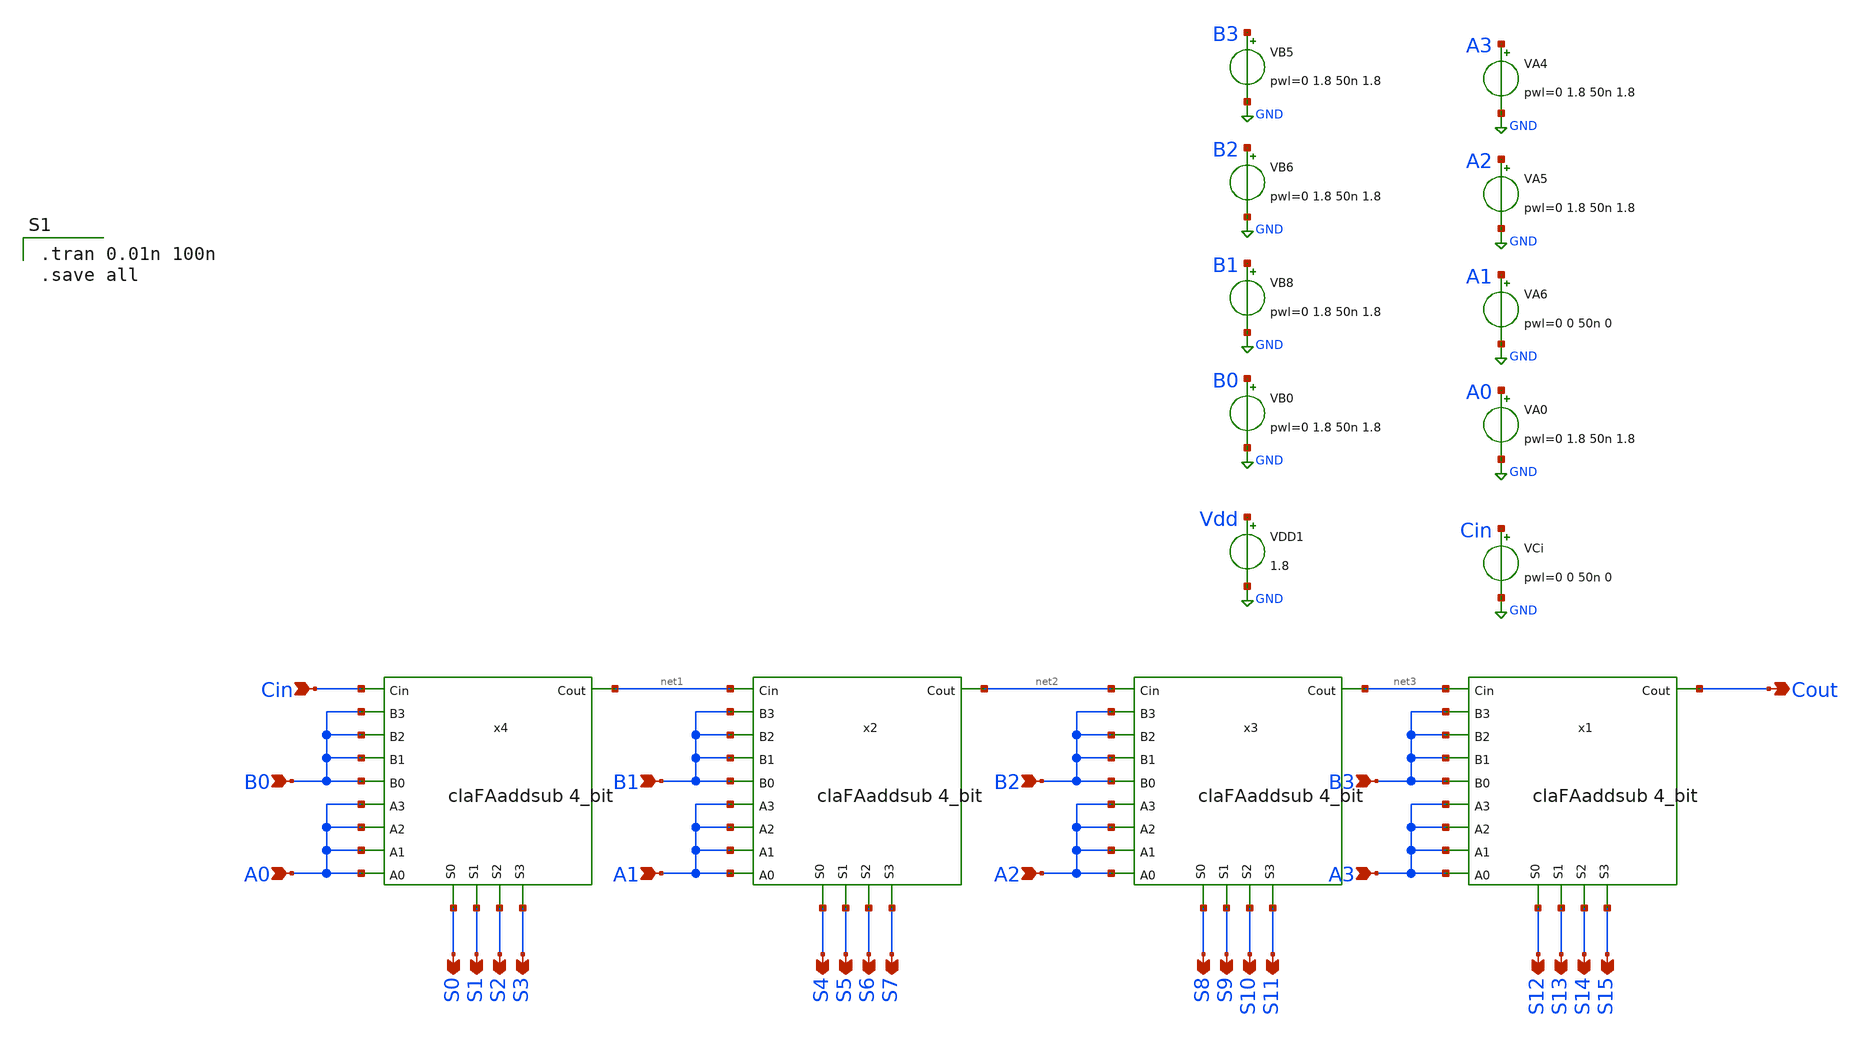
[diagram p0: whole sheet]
** sch_path: gates/32 bit addsubb cla.sch
**.subckt 32 bit addsubb cla B0 A0 B1 A1 B2 A2 B3 A3 S0 S1 S2 S3 S4 S5 S6 S7 S8 S9 S10 S11 S12 S13
*+ S14 S15 Cin Cout
*.ipin B0
*.ipin A0
*.ipin B1
*.ipin A1
*.ipin B2
*.ipin A2
*.ipin B3
*.ipin A3
*.opin S0
*.opin S1
*.opin S2
*.opin S3
*.opin S4
*.opin S5
*.opin S6
*.opin S7
*.opin S8
*.opin S9
*.opin S10
*.opin S11
*.opin S12
*.opin S13
*.opin S14
*.opin S15
*.ipin Cin
*.opin Cout
x1 B3 B3 B3 B3 A3 A3 A3 A3 S14 S13 S12 S15 net3 Cout claFAaddsub 4_bit
x2 B1 B1 B1 B1 A1 A1 A1 A1 S6 S5 S4 S7 net1 net2 claFAaddsub 4_bit
x3 B2 B2 B2 B2 A2 A2 A2 A2 S10 S9 S8 S11 net2 net3 claFAaddsub 4_bit
x4 B0 B0 B0 B0 A0 A0 A0 A0 S2 S1 S0 S3 Cin net1 claFAaddsub 4_bit
VA4 A3 GND pwl=0 1.8 50n 1.8
VA5 A2 GND pwl=0 1.8 50n 1.8
VA6 A1 GND pwl=0 0 50n 0
VA0 A0 GND pwl=0 1.8 50n 1.8
VB5 B3 GND pwl=0 1.8 50n 1.8
VB6 B2 GND pwl=0 1.8 50n 1.8
VB8 B1 GND pwl=0 1.8 50n 1.8
VB0 B0 GND pwl=0 1.8 50n 1.8
VCi Cin GND pwl=0 0 50n 0
VDD1 Vdd GND 1.8
**** begin user architecture code

.tran 0.01n 100n
.save all

.lib $::SKYWATER_MODELS/sky130.lib.spice tt
**** end user architecture code
**.ends

* expanding   symbol:  claFAaddsub 4_bit.sym # of pins=14
** sym_path: gates/claFAaddsub 4_bit.sym
** sch_path: gates/claFAaddsub 4_bit.sch
.subckt claFAaddsub 4_bit B2 B1 B0 B3 A2 A1 A0 A3 S2 S1 S0 S3 Cin Cout
*.opin S0
*.ipin A0
*.ipin B0
*.ipin Cin
*.opin S1
*.ipin A1
*.ipin B1
*.opin S2
*.ipin A2
*.ipin B2
*.opin S3
*.ipin A3
*.ipin B3
*.opin Cout
x1 A0 net4 net3 XOR2
x2 net3 Cin S0 XOR2
x3 net1 Co1 net2 OR2
x4 Cin net1 net3 AND2
x5 A0 net2 net4 AND2
x6 A1 net8 net7 XOR2
x7 net7 C1 S1 XOR2
x8 net5 Co2 net6 OR2
x9 C1 net5 net7 AND2
x10 A1 net6 net8 AND2
x11 A2 net12 net11 XOR2
x12 net11 C2 S2 XOR2
x13 net9 Co3 net10 OR2
x14 C2 net9 net11 AND2
x15 A2 net10 net12 AND2
x16 A3 net14 net13 XOR2
x17 net13 C3 S3 XOR2
x18 net15 Co4 net16 OR2
x19 C3 net15 net13 AND2
x20 A3 net16 net14 AND2
x21 net7 net6 net13 net3 net11 net10 net16 Cin net2 C1 C2 C3 Cout 4_BIT_CLA_Carry_logic
x22 Cin B0 net4 XOR2
x23 Cin B1 net8 XOR2
x24 Cin B2 net12 XOR2
x25 Cin B3 net14 XOR2
.ends


* expanding   symbol:  XOR2.sym # of pins=3
** sym_path: gates/XOR2.sym
** sch_path: gates/XOR2.sch
.subckt XOR2 B A Y
*.ipin A
*.ipin B
*.opin Y
XM1 Y A net5 GND sky130_fd_pr__nfet_01v8 L=0.15 W=1 nf=1 ad='int((nf+1)/2) * W/nf * 0.29' as='int((nf+2)/2) * W/nf * 0.29'
+ pd='2*int((nf+1)/2) * (W/nf + 0.29)' ps='2*int((nf+2)/2) * (W/nf + 0.29)' nrd='0.29 / W' nrs='0.29 / W'
+ sa=0 sb=0 sd=0 mult=1 m=1
XM2 net5 B GND GND sky130_fd_pr__nfet_01v8 L=0.15 W=1 nf=1 ad='int((nf+1)/2) * W/nf * 0.29' as='int((nf+2)/2) * W/nf * 0.29'
+ pd='2*int((nf+1)/2) * (W/nf + 0.29)' ps='2*int((nf+2)/2) * (W/nf + 0.29)' nrd='0.29 / W' nrs='0.29 / W'
+ sa=0 sb=0 sd=0 mult=1 m=1
XM3 Y net1 net2 VDD sky130_fd_pr__pfet_01v8 L=0.15 W=1 nf=1 ad='int((nf+1)/2) * W/nf * 0.29' as='int((nf+2)/2) * W/nf * 0.29'
+ pd='2*int((nf+1)/2) * (W/nf + 0.29)' ps='2*int((nf+2)/2) * (W/nf + 0.29)' nrd='0.29 / W' nrs='0.29 / W'
+ sa=0 sb=0 sd=0 mult=1 m=1
XM4 net2 A VDD VDD sky130_fd_pr__pfet_01v8 L=0.15 W=1 nf=1 ad='int((nf+1)/2) * W/nf * 0.29' as='int((nf+2)/2) * W/nf * 0.29'
+ pd='2*int((nf+1)/2) * (W/nf + 0.29)' ps='2*int((nf+2)/2) * (W/nf + 0.29)' nrd='0.29 / W' nrs='0.29 / W'
+ sa=0 sb=0 sd=0 mult=1 m=1
XM5 net2 B VDD VDD sky130_fd_pr__pfet_01v8 L=0.15 W=1 nf=1 ad='int((nf+1)/2) * W/nf * 0.29' as='int((nf+2)/2) * W/nf * 0.29'
+ pd='2*int((nf+1)/2) * (W/nf + 0.29)' ps='2*int((nf+2)/2) * (W/nf + 0.29)' nrd='0.29 / W' nrs='0.29 / W'
+ sa=0 sb=0 sd=0 mult=1 m=1
XM6 Y net3 net2 VDD sky130_fd_pr__pfet_01v8 L=0.15 W=1 nf=1 ad='int((nf+1)/2) * W/nf * 0.29' as='int((nf+2)/2) * W/nf * 0.29'
+ pd='2*int((nf+1)/2) * (W/nf + 0.29)' ps='2*int((nf+2)/2) * (W/nf + 0.29)' nrd='0.29 / W' nrs='0.29 / W'
+ sa=0 sb=0 sd=0 mult=1 m=1
XM7 Y net1 net4 GND sky130_fd_pr__nfet_01v8 L=0.15 W=1 nf=1 ad='int((nf+1)/2) * W/nf * 0.29' as='int((nf+2)/2) * W/nf * 0.29'
+ pd='2*int((nf+1)/2) * (W/nf + 0.29)' ps='2*int((nf+2)/2) * (W/nf + 0.29)' nrd='0.29 / W' nrs='0.29 / W'
+ sa=0 sb=0 sd=0 mult=1 m=1
XM8 net4 net3 GND GND sky130_fd_pr__nfet_01v8 L=0.15 W=1 nf=1 ad='int((nf+1)/2) * W/nf * 0.29' as='int((nf+2)/2) * W/nf * 0.29'
+ pd='2*int((nf+1)/2) * (W/nf + 0.29)' ps='2*int((nf+2)/2) * (W/nf + 0.29)' nrd='0.29 / W' nrs='0.29 / W'
+ sa=0 sb=0 sd=0 mult=1 m=1
X1 A net1 inv_vtc
X2 B net3 inv_vtc
.ends


* expanding   symbol:  OR2.sym # of pins=3
** sym_path: gates/OR2.sym
** sch_path: gates/OR2.sch
.subckt OR2 B Y A
*.ipin A
*.ipin B
*.opin Y
XM7 VDD B net2 VDD sky130_fd_pr__pfet_01v8 L=0.15 W=1 nf=1 ad='int((nf+1)/2) * W/nf * 0.29' as='int((nf+2)/2) * W/nf * 0.29'
+ pd='2*int((nf+1)/2) * (W/nf + 0.29)' ps='2*int((nf+2)/2) * (W/nf + 0.29)' nrd='0.29 / W' nrs='0.29 / W'
+ sa=0 sb=0 sd=0 mult=1 m=1
XM8 GND B net1 GND sky130_fd_pr__nfet_01v8 L=0.15 W=1 nf=1 ad='int((nf+1)/2) * W/nf * 0.29' as='int((nf+2)/2) * W/nf * 0.29'
+ pd='2*int((nf+1)/2) * (W/nf + 0.29)' ps='2*int((nf+2)/2) * (W/nf + 0.29)' nrd='0.29 / W' nrs='0.29 / W'
+ sa=0 sb=0 sd=0 mult=1 m=1
XM9 net2 A net1 VDD sky130_fd_pr__pfet_01v8 L=0.15 W=1 nf=1 ad='int((nf+1)/2) * W/nf * 0.29' as='int((nf+2)/2) * W/nf * 0.29'
+ pd='2*int((nf+1)/2) * (W/nf + 0.29)' ps='2*int((nf+2)/2) * (W/nf + 0.29)' nrd='0.29 / W' nrs='0.29 / W'
+ sa=0 sb=0 sd=0 mult=1 m=1
XM10 GND A net1 GND sky130_fd_pr__nfet_01v8 L=0.15 W=1 nf=1 ad='int((nf+1)/2) * W/nf * 0.29' as='int((nf+2)/2) * W/nf * 0.29'
+ pd='2*int((nf+1)/2) * (W/nf + 0.29)' ps='2*int((nf+2)/2) * (W/nf + 0.29)' nrd='0.29 / W' nrs='0.29 / W'
+ sa=0 sb=0 sd=0 mult=1 m=1
X1 net1 Y inv_vtc
.ends


* expanding   symbol:  AND2.sym # of pins=3
** sym_path: gates/AND2.sym
** sch_path: gates/AND2.sch
.subckt AND2 A Y B
*.opin Y
*.ipin A
*.ipin B
x1 A net1 B NAND2_Gate
X2 net1 Y inv_vtc
.ends


* expanding   symbol:  4_BIT_CLA_Carry_logic.sym # of pins=13
** sym_path: gates/4_BIT_CLA_Carry_logic.sym
** sch_path: gates/4_BIT_CLA_Carry_logic.sch
.subckt 4_BIT_CLA_Carry_logic P1 G1 P3 P0 P2 G2 G3 Cin G0 C1 C2 C3 C4
*.ipin P0
*.ipin P1
*.ipin P2
*.ipin P3
*.ipin G0
*.ipin G1
*.ipin G2
*.ipin G3
*.ipin Cin
*.opin C1
*.opin C2
*.opin C3
*.opin C4
x5 Cin x5 P0 AND2
x6 G0 C1 x5 OR2
x7 G1 net1 net2 C2 OR3
x8 P1 net1 G0 AND2
x9 Cin net10 P0 P1 AND3
x1 G2 net3 net4 C3 net5 OR4
x2 P2 net3 G1 AND2
x3 P1 net11 P2 G0 AND3
x4 net12 net5 net13 net14 net15 AND4
x10 G3 net6 net7 net8 C4 net9 OR5
x12 P3 net6 G2 AND2
x13 net16 net17 net18 net19 AND3
x14 net20 net8 net21 net22 net23 AND4
x11 net24 net25 net26 net27 net28 net29 AND5
.ends


* expanding   symbol:  inv_vtc.sym # of pins=2
** sym_path: gates/inv_vtc.sym
** sch_path: gates/inv_vtc.sch
.subckt inv_vtc A Y
*.ipin A
*.opin Y
XM1 Y A VDD VDD sky130_fd_pr__pfet_01v8 L=0.15 W=2 nf=1 ad='int((nf+1)/2) * W/nf * 0.29' as='int((nf+2)/2) * W/nf * 0.29'
+ pd='2*int((nf+1)/2) * (W/nf + 0.29)' ps='2*int((nf+2)/2) * (W/nf + 0.29)' nrd='0.29 / W' nrs='0.29 / W'
+ sa=0 sb=0 sd=0 mult=1 m=1
XM2 Y A GND GND sky130_fd_pr__nfet_01v8 L=0.15 W=1 nf=1 ad='int((nf+1)/2) * W/nf * 0.29' as='int((nf+2)/2) * W/nf * 0.29'
+ pd='2*int((nf+1)/2) * (W/nf + 0.29)' ps='2*int((nf+2)/2) * (W/nf + 0.29)' nrd='0.29 / W' nrs='0.29 / W'
+ sa=0 sb=0 sd=0 mult=1 m=1
.ends


* expanding   symbol:  NAND2_Gate.sym # of pins=3
** sym_path: gates/NAND2_Gate.sym
** sch_path: gates/NAND2_Gate.sch
.subckt NAND2_Gate A Y B
*.ipin A
*.ipin B
*.opin Y
XM1 Y A net1 GND sky130_fd_pr__nfet_01v8 L=0.15 W=1 nf=1 ad='int((nf+1)/2) * W/nf * 0.29' as='int((nf+2)/2) * W/nf * 0.29'
+ pd='2*int((nf+1)/2) * (W/nf + 0.29)' ps='2*int((nf+2)/2) * (W/nf + 0.29)' nrd='0.29 / W' nrs='0.29 / W'
+ sa=0 sb=0 sd=0 mult=1 m=1
XM2 net1 B GND GND sky130_fd_pr__nfet_01v8 L=0.15 W=1 nf=1 ad='int((nf+1)/2) * W/nf * 0.29' as='int((nf+2)/2) * W/nf * 0.29'
+ pd='2*int((nf+1)/2) * (W/nf + 0.29)' ps='2*int((nf+2)/2) * (W/nf + 0.29)' nrd='0.29 / W' nrs='0.29 / W'
+ sa=0 sb=0 sd=0 mult=1 m=1
XM3 Y A VDD VDD sky130_fd_pr__pfet_01v8 L=0.15 W=1 nf=1 ad='int((nf+1)/2) * W/nf * 0.29' as='int((nf+2)/2) * W/nf * 0.29'
+ pd='2*int((nf+1)/2) * (W/nf + 0.29)' ps='2*int((nf+2)/2) * (W/nf + 0.29)' nrd='0.29 / W' nrs='0.29 / W'
+ sa=0 sb=0 sd=0 mult=1 m=1
XM4 Y B VDD VDD sky130_fd_pr__pfet_01v8 L=0.15 W=1 nf=1 ad='int((nf+1)/2) * W/nf * 0.29' as='int((nf+2)/2) * W/nf * 0.29'
+ pd='2*int((nf+1)/2) * (W/nf + 0.29)' ps='2*int((nf+2)/2) * (W/nf + 0.29)' nrd='0.29 / W' nrs='0.29 / W'
+ sa=0 sb=0 sd=0 mult=1 m=1
.ends


* expanding   symbol:  OR3.sym # of pins=4
** sym_path: gates/OR3.sym
** sch_path: gates/OR3.sch
.subckt OR3 C B A Y
*.ipin A
*.ipin B
*.opin Y
*.ipin C
XM5 VDD C net3 VDD sky130_fd_pr__pfet_01v8 L=0.15 W=1 nf=1 ad='int((nf+1)/2) * W/nf * 0.29' as='int((nf+2)/2) * W/nf * 0.29'
+ pd='2*int((nf+1)/2) * (W/nf + 0.29)' ps='2*int((nf+2)/2) * (W/nf + 0.29)' nrd='0.29 / W' nrs='0.29 / W'
+ sa=0 sb=0 sd=0 mult=1 m=1
XM6 GND C net1 GND sky130_fd_pr__nfet_01v8 L=0.15 W=1 nf=1 ad='int((nf+1)/2) * W/nf * 0.29' as='int((nf+2)/2) * W/nf * 0.29'
+ pd='2*int((nf+1)/2) * (W/nf + 0.29)' ps='2*int((nf+2)/2) * (W/nf + 0.29)' nrd='0.29 / W' nrs='0.29 / W'
+ sa=0 sb=0 sd=0 mult=1 m=1
XM7 net3 B net2 VDD sky130_fd_pr__pfet_01v8 L=0.15 W=1 nf=1 ad='int((nf+1)/2) * W/nf * 0.29' as='int((nf+2)/2) * W/nf * 0.29'
+ pd='2*int((nf+1)/2) * (W/nf + 0.29)' ps='2*int((nf+2)/2) * (W/nf + 0.29)' nrd='0.29 / W' nrs='0.29 / W'
+ sa=0 sb=0 sd=0 mult=1 m=1
XM8 GND B net1 GND sky130_fd_pr__nfet_01v8 L=0.15 W=1 nf=1 ad='int((nf+1)/2) * W/nf * 0.29' as='int((nf+2)/2) * W/nf * 0.29'
+ pd='2*int((nf+1)/2) * (W/nf + 0.29)' ps='2*int((nf+2)/2) * (W/nf + 0.29)' nrd='0.29 / W' nrs='0.29 / W'
+ sa=0 sb=0 sd=0 mult=1 m=1
XM9 net2 A net1 VDD sky130_fd_pr__pfet_01v8 L=0.15 W=1 nf=1 ad='int((nf+1)/2) * W/nf * 0.29' as='int((nf+2)/2) * W/nf * 0.29'
+ pd='2*int((nf+1)/2) * (W/nf + 0.29)' ps='2*int((nf+2)/2) * (W/nf + 0.29)' nrd='0.29 / W' nrs='0.29 / W'
+ sa=0 sb=0 sd=0 mult=1 m=1
XM10 GND A net1 GND sky130_fd_pr__nfet_01v8 L=0.15 W=1 nf=1 ad='int((nf+1)/2) * W/nf * 0.29' as='int((nf+2)/2) * W/nf * 0.29'
+ pd='2*int((nf+1)/2) * (W/nf + 0.29)' ps='2*int((nf+2)/2) * (W/nf + 0.29)' nrd='0.29 / W' nrs='0.29 / W'
+ sa=0 sb=0 sd=0 mult=1 m=1
X1 net1 Y inv_vtc
.ends


* expanding   symbol:  AND3.sym # of pins=4
** sym_path: gates/AND3.sym
** sch_path: gates/AND3.sch
.subckt AND3 A Y B c
*.ipin A
*.ipin B
*.opin Y
*.ipin c
XM1 net1 A net2 GND sky130_fd_pr__nfet_01v8 L=0.15 W=1 nf=1 ad='int((nf+1)/2) * W/nf * 0.29' as='int((nf+2)/2) * W/nf * 0.29'
+ pd='2*int((nf+1)/2) * (W/nf + 0.29)' ps='2*int((nf+2)/2) * (W/nf + 0.29)' nrd='0.29 / W' nrs='0.29 / W'
+ sa=0 sb=0 sd=0 mult=1 m=1
XM2 net2 B net3 GND sky130_fd_pr__nfet_01v8 L=0.15 W=1 nf=1 ad='int((nf+1)/2) * W/nf * 0.29' as='int((nf+2)/2) * W/nf * 0.29'
+ pd='2*int((nf+1)/2) * (W/nf + 0.29)' ps='2*int((nf+2)/2) * (W/nf + 0.29)' nrd='0.29 / W' nrs='0.29 / W'
+ sa=0 sb=0 sd=0 mult=1 m=1
XM3 net1 A VDD VDD sky130_fd_pr__pfet_01v8 L=0.15 W=1 nf=1 ad='int((nf+1)/2) * W/nf * 0.29' as='int((nf+2)/2) * W/nf * 0.29'
+ pd='2*int((nf+1)/2) * (W/nf + 0.29)' ps='2*int((nf+2)/2) * (W/nf + 0.29)' nrd='0.29 / W' nrs='0.29 / W'
+ sa=0 sb=0 sd=0 mult=1 m=1
XM4 net1 B VDD VDD sky130_fd_pr__pfet_01v8 L=0.15 W=1 nf=1 ad='int((nf+1)/2) * W/nf * 0.29' as='int((nf+2)/2) * W/nf * 0.29'
+ pd='2*int((nf+1)/2) * (W/nf + 0.29)' ps='2*int((nf+2)/2) * (W/nf + 0.29)' nrd='0.29 / W' nrs='0.29 / W'
+ sa=0 sb=0 sd=0 mult=1 m=1
XM5 net1 c VDD VDD sky130_fd_pr__pfet_01v8 L=0.15 W=1 nf=1 ad='int((nf+1)/2) * W/nf * 0.29' as='int((nf+2)/2) * W/nf * 0.29'
+ pd='2*int((nf+1)/2) * (W/nf + 0.29)' ps='2*int((nf+2)/2) * (W/nf + 0.29)' nrd='0.29 / W' nrs='0.29 / W'
+ sa=0 sb=0 sd=0 mult=1 m=1
XM6 net3 c GND GND sky130_fd_pr__nfet_01v8 L=0.15 W=1 nf=1 ad='int((nf+1)/2) * W/nf * 0.29' as='int((nf+2)/2) * W/nf * 0.29'
+ pd='2*int((nf+1)/2) * (W/nf + 0.29)' ps='2*int((nf+2)/2) * (W/nf + 0.29)' nrd='0.29 / W' nrs='0.29 / W'
+ sa=0 sb=0 sd=0 mult=1 m=1
X1 net1 Y inv_vtc
.ends


* expanding   symbol:  OR4.sym # of pins=5
** sym_path: gates/OR4.sym
** sch_path: gates/OR4.sch
.subckt OR4 D C B Y A
*.ipin A
*.ipin B
*.opin Y
*.ipin C
*.ipin D
XM2 GND D net1 GND sky130_fd_pr__nfet_01v8 L=0.15 W=1 nf=1 ad='int((nf+1)/2) * W/nf * 0.29' as='int((nf+2)/2) * W/nf * 0.29'
+ pd='2*int((nf+1)/2) * (W/nf + 0.29)' ps='2*int((nf+2)/2) * (W/nf + 0.29)' nrd='0.29 / W' nrs='0.29 / W'
+ sa=0 sb=0 sd=0 mult=1 m=1
XM4 VDD D net4 VDD sky130_fd_pr__pfet_01v8 L=0.15 W=1 nf=1 ad='int((nf+1)/2) * W/nf * 0.29' as='int((nf+2)/2) * W/nf * 0.29'
+ pd='2*int((nf+1)/2) * (W/nf + 0.29)' ps='2*int((nf+2)/2) * (W/nf + 0.29)' nrd='0.29 / W' nrs='0.29 / W'
+ sa=0 sb=0 sd=0 mult=1 m=1
XM5 net4 C net3 VDD sky130_fd_pr__pfet_01v8 L=0.15 W=1 nf=1 ad='int((nf+1)/2) * W/nf * 0.29' as='int((nf+2)/2) * W/nf * 0.29'
+ pd='2*int((nf+1)/2) * (W/nf + 0.29)' ps='2*int((nf+2)/2) * (W/nf + 0.29)' nrd='0.29 / W' nrs='0.29 / W'
+ sa=0 sb=0 sd=0 mult=1 m=1
XM6 GND C net1 GND sky130_fd_pr__nfet_01v8 L=0.15 W=1 nf=1 ad='int((nf+1)/2) * W/nf * 0.29' as='int((nf+2)/2) * W/nf * 0.29'
+ pd='2*int((nf+1)/2) * (W/nf + 0.29)' ps='2*int((nf+2)/2) * (W/nf + 0.29)' nrd='0.29 / W' nrs='0.29 / W'
+ sa=0 sb=0 sd=0 mult=1 m=1
XM7 net3 B net2 VDD sky130_fd_pr__pfet_01v8 L=0.15 W=1 nf=1 ad='int((nf+1)/2) * W/nf * 0.29' as='int((nf+2)/2) * W/nf * 0.29'
+ pd='2*int((nf+1)/2) * (W/nf + 0.29)' ps='2*int((nf+2)/2) * (W/nf + 0.29)' nrd='0.29 / W' nrs='0.29 / W'
+ sa=0 sb=0 sd=0 mult=1 m=1
XM8 GND B net1 GND sky130_fd_pr__nfet_01v8 L=0.15 W=1 nf=1 ad='int((nf+1)/2) * W/nf * 0.29' as='int((nf+2)/2) * W/nf * 0.29'
+ pd='2*int((nf+1)/2) * (W/nf + 0.29)' ps='2*int((nf+2)/2) * (W/nf + 0.29)' nrd='0.29 / W' nrs='0.29 / W'
+ sa=0 sb=0 sd=0 mult=1 m=1
XM9 net2 A net1 VDD sky130_fd_pr__pfet_01v8 L=0.15 W=1 nf=1 ad='int((nf+1)/2) * W/nf * 0.29' as='int((nf+2)/2) * W/nf * 0.29'
+ pd='2*int((nf+1)/2) * (W/nf + 0.29)' ps='2*int((nf+2)/2) * (W/nf + 0.29)' nrd='0.29 / W' nrs='0.29 / W'
+ sa=0 sb=0 sd=0 mult=1 m=1
XM10 GND A net1 GND sky130_fd_pr__nfet_01v8 L=0.15 W=1 nf=1 ad='int((nf+1)/2) * W/nf * 0.29' as='int((nf+2)/2) * W/nf * 0.29'
+ pd='2*int((nf+1)/2) * (W/nf + 0.29)' ps='2*int((nf+2)/2) * (W/nf + 0.29)' nrd='0.29 / W' nrs='0.29 / W'
+ sa=0 sb=0 sd=0 mult=1 m=1
X2 net1 Y inv_vtc
.ends


* expanding   symbol:  AND4.sym # of pins=5
** sym_path: gates/AND4.sym
** sch_path: gates/AND4.sch
.subckt AND4 A Y B C D
*.ipin A
*.ipin B
*.opin Y
*.ipin C
*.ipin D
XM1 net1 A net2 GND sky130_fd_pr__nfet_01v8 L=0.15 W=1 nf=1 ad='int((nf+1)/2) * W/nf * 0.29' as='int((nf+2)/2) * W/nf * 0.29'
+ pd='2*int((nf+1)/2) * (W/nf + 0.29)' ps='2*int((nf+2)/2) * (W/nf + 0.29)' nrd='0.29 / W' nrs='0.29 / W'
+ sa=0 sb=0 sd=0 mult=1 m=1
XM2 net2 B net3 GND sky130_fd_pr__nfet_01v8 L=0.15 W=1 nf=1 ad='int((nf+1)/2) * W/nf * 0.29' as='int((nf+2)/2) * W/nf * 0.29'
+ pd='2*int((nf+1)/2) * (W/nf + 0.29)' ps='2*int((nf+2)/2) * (W/nf + 0.29)' nrd='0.29 / W' nrs='0.29 / W'
+ sa=0 sb=0 sd=0 mult=1 m=1
XM3 net1 A VDD VDD sky130_fd_pr__pfet_01v8 L=0.15 W=1 nf=1 ad='int((nf+1)/2) * W/nf * 0.29' as='int((nf+2)/2) * W/nf * 0.29'
+ pd='2*int((nf+1)/2) * (W/nf + 0.29)' ps='2*int((nf+2)/2) * (W/nf + 0.29)' nrd='0.29 / W' nrs='0.29 / W'
+ sa=0 sb=0 sd=0 mult=1 m=1
XM4 net1 B VDD VDD sky130_fd_pr__pfet_01v8 L=0.15 W=1 nf=1 ad='int((nf+1)/2) * W/nf * 0.29' as='int((nf+2)/2) * W/nf * 0.29'
+ pd='2*int((nf+1)/2) * (W/nf + 0.29)' ps='2*int((nf+2)/2) * (W/nf + 0.29)' nrd='0.29 / W' nrs='0.29 / W'
+ sa=0 sb=0 sd=0 mult=1 m=1
XM5 net1 C VDD VDD sky130_fd_pr__pfet_01v8 L=0.15 W=1 nf=1 ad='int((nf+1)/2) * W/nf * 0.29' as='int((nf+2)/2) * W/nf * 0.29'
+ pd='2*int((nf+1)/2) * (W/nf + 0.29)' ps='2*int((nf+2)/2) * (W/nf + 0.29)' nrd='0.29 / W' nrs='0.29 / W'
+ sa=0 sb=0 sd=0 mult=1 m=1
XM6 net3 C net4 GND sky130_fd_pr__nfet_01v8 L=0.15 W=1 nf=1 ad='int((nf+1)/2) * W/nf * 0.29' as='int((nf+2)/2) * W/nf * 0.29'
+ pd='2*int((nf+1)/2) * (W/nf + 0.29)' ps='2*int((nf+2)/2) * (W/nf + 0.29)' nrd='0.29 / W' nrs='0.29 / W'
+ sa=0 sb=0 sd=0 mult=1 m=1
XM7 net1 D VDD VDD sky130_fd_pr__pfet_01v8 L=0.15 W=1 nf=1 ad='int((nf+1)/2) * W/nf * 0.29' as='int((nf+2)/2) * W/nf * 0.29'
+ pd='2*int((nf+1)/2) * (W/nf + 0.29)' ps='2*int((nf+2)/2) * (W/nf + 0.29)' nrd='0.29 / W' nrs='0.29 / W'
+ sa=0 sb=0 sd=0 mult=1 m=1
XM8 net4 D GND GND sky130_fd_pr__nfet_01v8 L=0.15 W=1 nf=1 ad='int((nf+1)/2) * W/nf * 0.29' as='int((nf+2)/2) * W/nf * 0.29'
+ pd='2*int((nf+1)/2) * (W/nf + 0.29)' ps='2*int((nf+2)/2) * (W/nf + 0.29)' nrd='0.29 / W' nrs='0.29 / W'
+ sa=0 sb=0 sd=0 mult=1 m=1
X1 net1 Y inv_vtc
.ends


* expanding   symbol:  OR5.sym # of pins=6
** sym_path: gates/OR5.sym
** sch_path: gates/OR5.sch
.subckt OR5 E D C B Y A
*.ipin A
*.ipin B
*.opin Y
*.ipin C
*.ipin D
*.ipin E
XM1 GND E net1 GND sky130_fd_pr__nfet_01v8 L=0.15 W=1 nf=1 ad='int((nf+1)/2) * W/nf * 0.29' as='int((nf+2)/2) * W/nf * 0.29'
+ pd='2*int((nf+1)/2) * (W/nf + 0.29)' ps='2*int((nf+2)/2) * (W/nf + 0.29)' nrd='0.29 / W' nrs='0.29 / W'
+ sa=0 sb=0 sd=0 mult=1 m=1
XM2 GND D net1 GND sky130_fd_pr__nfet_01v8 L=0.15 W=1 nf=1 ad='int((nf+1)/2) * W/nf * 0.29' as='int((nf+2)/2) * W/nf * 0.29'
+ pd='2*int((nf+1)/2) * (W/nf + 0.29)' ps='2*int((nf+2)/2) * (W/nf + 0.29)' nrd='0.29 / W' nrs='0.29 / W'
+ sa=0 sb=0 sd=0 mult=1 m=1
XM3 VDD E VDD VDD sky130_fd_pr__pfet_01v8 L=0.15 W=1 nf=1 ad='int((nf+1)/2) * W/nf * 0.29' as='int((nf+2)/2) * W/nf * 0.29'
+ pd='2*int((nf+1)/2) * (W/nf + 0.29)' ps='2*int((nf+2)/2) * (W/nf + 0.29)' nrd='0.29 / W' nrs='0.29 / W'
+ sa=0 sb=0 sd=0 mult=1 m=1
XM4 VDD D net4 VDD sky130_fd_pr__pfet_01v8 L=0.15 W=1 nf=1 ad='int((nf+1)/2) * W/nf * 0.29' as='int((nf+2)/2) * W/nf * 0.29'
+ pd='2*int((nf+1)/2) * (W/nf + 0.29)' ps='2*int((nf+2)/2) * (W/nf + 0.29)' nrd='0.29 / W' nrs='0.29 / W'
+ sa=0 sb=0 sd=0 mult=1 m=1
XM5 net4 C net3 VDD sky130_fd_pr__pfet_01v8 L=0.15 W=1 nf=1 ad='int((nf+1)/2) * W/nf * 0.29' as='int((nf+2)/2) * W/nf * 0.29'
+ pd='2*int((nf+1)/2) * (W/nf + 0.29)' ps='2*int((nf+2)/2) * (W/nf + 0.29)' nrd='0.29 / W' nrs='0.29 / W'
+ sa=0 sb=0 sd=0 mult=1 m=1
XM6 GND C net1 GND sky130_fd_pr__nfet_01v8 L=0.15 W=1 nf=1 ad='int((nf+1)/2) * W/nf * 0.29' as='int((nf+2)/2) * W/nf * 0.29'
+ pd='2*int((nf+1)/2) * (W/nf + 0.29)' ps='2*int((nf+2)/2) * (W/nf + 0.29)' nrd='0.29 / W' nrs='0.29 / W'
+ sa=0 sb=0 sd=0 mult=1 m=1
XM7 net3 B net2 VDD sky130_fd_pr__pfet_01v8 L=0.15 W=1 nf=1 ad='int((nf+1)/2) * W/nf * 0.29' as='int((nf+2)/2) * W/nf * 0.29'
+ pd='2*int((nf+1)/2) * (W/nf + 0.29)' ps='2*int((nf+2)/2) * (W/nf + 0.29)' nrd='0.29 / W' nrs='0.29 / W'
+ sa=0 sb=0 sd=0 mult=1 m=1
XM8 GND B net1 GND sky130_fd_pr__nfet_01v8 L=0.15 W=1 nf=1 ad='int((nf+1)/2) * W/nf * 0.29' as='int((nf+2)/2) * W/nf * 0.29'
+ pd='2*int((nf+1)/2) * (W/nf + 0.29)' ps='2*int((nf+2)/2) * (W/nf + 0.29)' nrd='0.29 / W' nrs='0.29 / W'
+ sa=0 sb=0 sd=0 mult=1 m=1
XM9 net2 A net1 VDD sky130_fd_pr__pfet_01v8 L=0.15 W=1 nf=1 ad='int((nf+1)/2) * W/nf * 0.29' as='int((nf+2)/2) * W/nf * 0.29'
+ pd='2*int((nf+1)/2) * (W/nf + 0.29)' ps='2*int((nf+2)/2) * (W/nf + 0.29)' nrd='0.29 / W' nrs='0.29 / W'
+ sa=0 sb=0 sd=0 mult=1 m=1
XM10 GND A net1 GND sky130_fd_pr__nfet_01v8 L=0.15 W=1 nf=1 ad='int((nf+1)/2) * W/nf * 0.29' as='int((nf+2)/2) * W/nf * 0.29'
+ pd='2*int((nf+1)/2) * (W/nf + 0.29)' ps='2*int((nf+2)/2) * (W/nf + 0.29)' nrd='0.29 / W' nrs='0.29 / W'
+ sa=0 sb=0 sd=0 mult=1 m=1
X2 net1 Y inv_vtc
.ends


* expanding   symbol:  AND5.sym # of pins=6
** sym_path: gates/AND5.sym
** sch_path: gates/AND5.sch
.subckt AND5 A Y B C D E
*.ipin A
*.ipin B
*.opin Y
*.ipin C
*.ipin D
*.ipin E
XM1 net1 A net2 GND sky130_fd_pr__nfet_01v8 L=0.15 W=1 nf=1 ad='int((nf+1)/2) * W/nf * 0.29' as='int((nf+2)/2) * W/nf * 0.29'
+ pd='2*int((nf+1)/2) * (W/nf + 0.29)' ps='2*int((nf+2)/2) * (W/nf + 0.29)' nrd='0.29 / W' nrs='0.29 / W'
+ sa=0 sb=0 sd=0 mult=1 m=1
XM2 net2 B net3 GND sky130_fd_pr__nfet_01v8 L=0.15 W=1 nf=1 ad='int((nf+1)/2) * W/nf * 0.29' as='int((nf+2)/2) * W/nf * 0.29'
+ pd='2*int((nf+1)/2) * (W/nf + 0.29)' ps='2*int((nf+2)/2) * (W/nf + 0.29)' nrd='0.29 / W' nrs='0.29 / W'
+ sa=0 sb=0 sd=0 mult=1 m=1
XM3 net1 A VDD VDD sky130_fd_pr__pfet_01v8 L=0.15 W=1 nf=1 ad='int((nf+1)/2) * W/nf * 0.29' as='int((nf+2)/2) * W/nf * 0.29'
+ pd='2*int((nf+1)/2) * (W/nf + 0.29)' ps='2*int((nf+2)/2) * (W/nf + 0.29)' nrd='0.29 / W' nrs='0.29 / W'
+ sa=0 sb=0 sd=0 mult=1 m=1
XM4 net1 B VDD VDD sky130_fd_pr__pfet_01v8 L=0.15 W=1 nf=1 ad='int((nf+1)/2) * W/nf * 0.29' as='int((nf+2)/2) * W/nf * 0.29'
+ pd='2*int((nf+1)/2) * (W/nf + 0.29)' ps='2*int((nf+2)/2) * (W/nf + 0.29)' nrd='0.29 / W' nrs='0.29 / W'
+ sa=0 sb=0 sd=0 mult=1 m=1
XM5 net1 C VDD VDD sky130_fd_pr__pfet_01v8 L=0.15 W=1 nf=1 ad='int((nf+1)/2) * W/nf * 0.29' as='int((nf+2)/2) * W/nf * 0.29'
+ pd='2*int((nf+1)/2) * (W/nf + 0.29)' ps='2*int((nf+2)/2) * (W/nf + 0.29)' nrd='0.29 / W' nrs='0.29 / W'
+ sa=0 sb=0 sd=0 mult=1 m=1
XM6 net3 C net4 GND sky130_fd_pr__nfet_01v8 L=0.15 W=1 nf=1 ad='int((nf+1)/2) * W/nf * 0.29' as='int((nf+2)/2) * W/nf * 0.29'
+ pd='2*int((nf+1)/2) * (W/nf + 0.29)' ps='2*int((nf+2)/2) * (W/nf + 0.29)' nrd='0.29 / W' nrs='0.29 / W'
+ sa=0 sb=0 sd=0 mult=1 m=1
XM7 net1 D VDD VDD sky130_fd_pr__pfet_01v8 L=0.15 W=1 nf=1 ad='int((nf+1)/2) * W/nf * 0.29' as='int((nf+2)/2) * W/nf * 0.29'
+ pd='2*int((nf+1)/2) * (W/nf + 0.29)' ps='2*int((nf+2)/2) * (W/nf + 0.29)' nrd='0.29 / W' nrs='0.29 / W'
+ sa=0 sb=0 sd=0 mult=1 m=1
XM8 net4 D GND GND sky130_fd_pr__nfet_01v8 L=0.15 W=1 nf=1 ad='int((nf+1)/2) * W/nf * 0.29' as='int((nf+2)/2) * W/nf * 0.29'
+ pd='2*int((nf+1)/2) * (W/nf + 0.29)' ps='2*int((nf+2)/2) * (W/nf + 0.29)' nrd='0.29 / W' nrs='0.29 / W'
+ sa=0 sb=0 sd=0 mult=1 m=1
XM9 net1 E VDD VDD sky130_fd_pr__pfet_01v8 L=0.15 W=1 nf=1 ad='int((nf+1)/2) * W/nf * 0.29' as='int((nf+2)/2) * W/nf * 0.29'
+ pd='2*int((nf+1)/2) * (W/nf + 0.29)' ps='2*int((nf+2)/2) * (W/nf + 0.29)' nrd='0.29 / W' nrs='0.29 / W'
+ sa=0 sb=0 sd=0 mult=1 m=1
XM10 GND E GND GND sky130_fd_pr__nfet_01v8 L=0.15 W=1 nf=1 ad='int((nf+1)/2) * W/nf * 0.29' as='int((nf+2)/2) * W/nf * 0.29'
+ pd='2*int((nf+1)/2) * (W/nf + 0.29)' ps='2*int((nf+2)/2) * (W/nf + 0.29)' nrd='0.29 / W' nrs='0.29 / W'
+ sa=0 sb=0 sd=0 mult=1 m=1
X1 net1 Y inv_vtc
.ends

.GLOBAL GND
.GLOBAL VDD
.end
